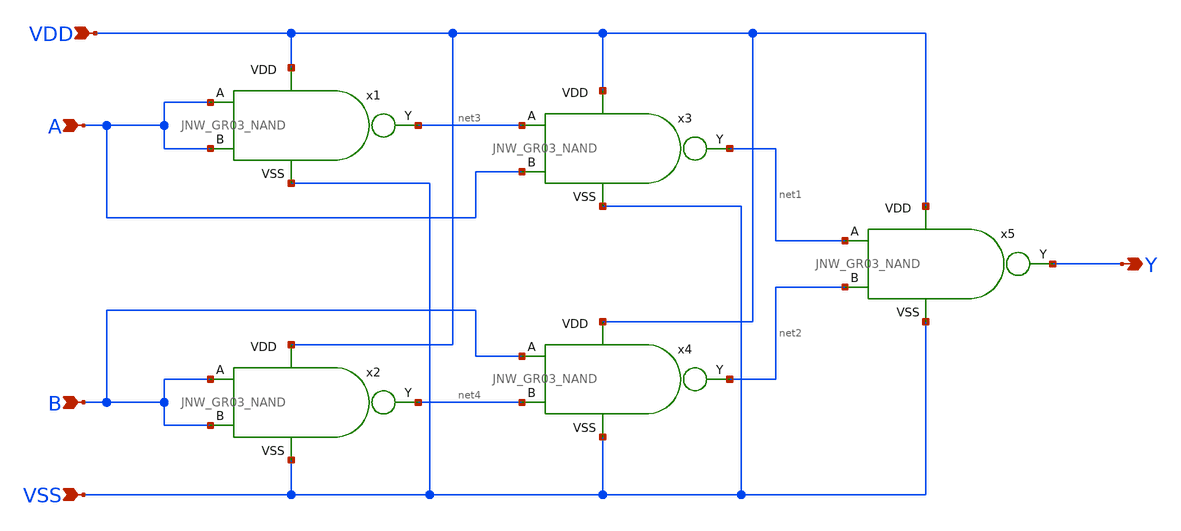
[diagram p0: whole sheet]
** sch_path: design/JNW_GR03_SKY130A/JNW_GR03_XOR.sch
**.subckt JNW_GR03_XOR VDD Y VSS A B
*.ipin VDD
*.opin Y
*.ipin VSS
*.ipin A
*.ipin B
x1 VDD net3 A A VSS JNW_GR03_NAND
x2 VDD net4 B B VSS JNW_GR03_NAND
x3 VDD net1 net3 A VSS JNW_GR03_NAND
x4 VDD net2 B net4 VSS JNW_GR03_NAND
x5 VDD Y net1 net2 VSS JNW_GR03_NAND
**.ends
.end
